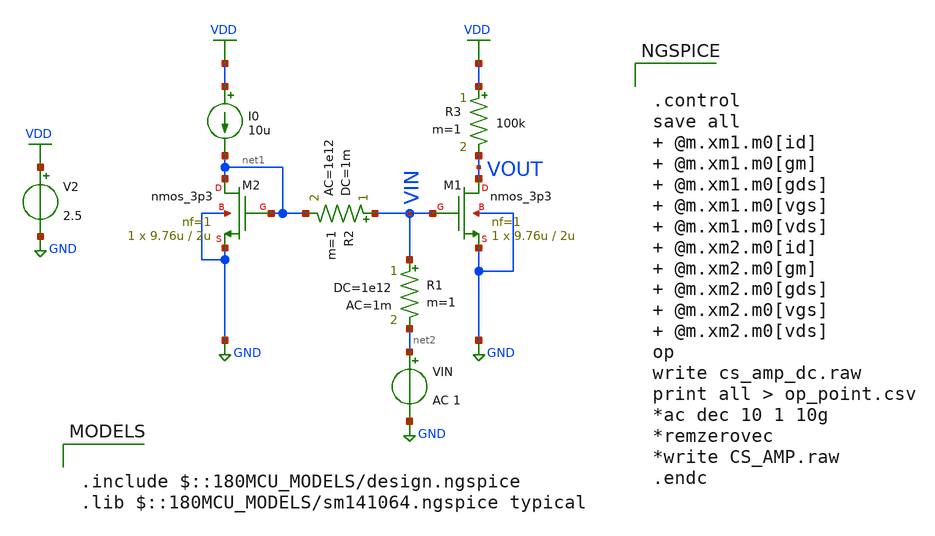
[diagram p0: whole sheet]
** sch_path: ITI_Labs/Lab2/Design/CS_Amp.sch
**.subckt CS_Amp
XM1 VOUT VIN GND GND nmos_3p3 L=2u W=9.76u nf=1 ad='int((nf+1)/2) * W/nf * 0.18u' as='int((nf+2)/2) * W/nf * 0.18u'
+ pd='2*int((nf+1)/2) * (W/nf + 0.18u)' ps='2*int((nf+2)/2) * (W/nf + 0.18u)' nrd='0.18u / W' nrs='0.18u / W'
+ sa=0 sb=0 sd=0 m=1
XM2 net1 net1 GND GND nmos_3p3 L=2u W=9.76u nf=1 ad='int((nf+1)/2) * W/nf * 0.18u' as='int((nf+2)/2) * W/nf * 0.18u'
+ pd='2*int((nf+1)/2) * (W/nf + 0.18u)' ps='2*int((nf+2)/2) * (W/nf + 0.18u)' nrd='0.18u / W' nrs='0.18u / W'
+ sa=0 sb=0 sd=0 m=1
R1 VIN net2 1e12 ac=1m m=1
R2 VIN net1 1m ac=1e12 m=1
I0 VDD net1 10u
VIN net2 GND AC 1
V2 VDD GND 2.5
R3 VDD VOUT 100k m=1
**** begin user architecture code

.include $::180MCU_MODELS/design.ngspice
.lib $::180MCU_MODELS/sm141064.ngspice typical



.control
save all  @m.xm1.m0[id]  @m.xm1.m0[gm]  @m.xm1.m0[gds]  @m.xm1.m0[vgs]  @m.xm1.m0[vds]
+  @m.xm2.m0[id]  @m.xm2.m0[gm]  @m.xm2.m0[gds]  @m.xm2.m0[vgs]  @m.xm2.m0[vds]
op
write cs_amp_dc.raw
print all > op_point.csv
*ac dec 10 1 10g
*remzerovec
*write CS_AMP.raw
.endc


**** end user architecture code
**.ends
.GLOBAL GND
.GLOBAL VDD
.end
